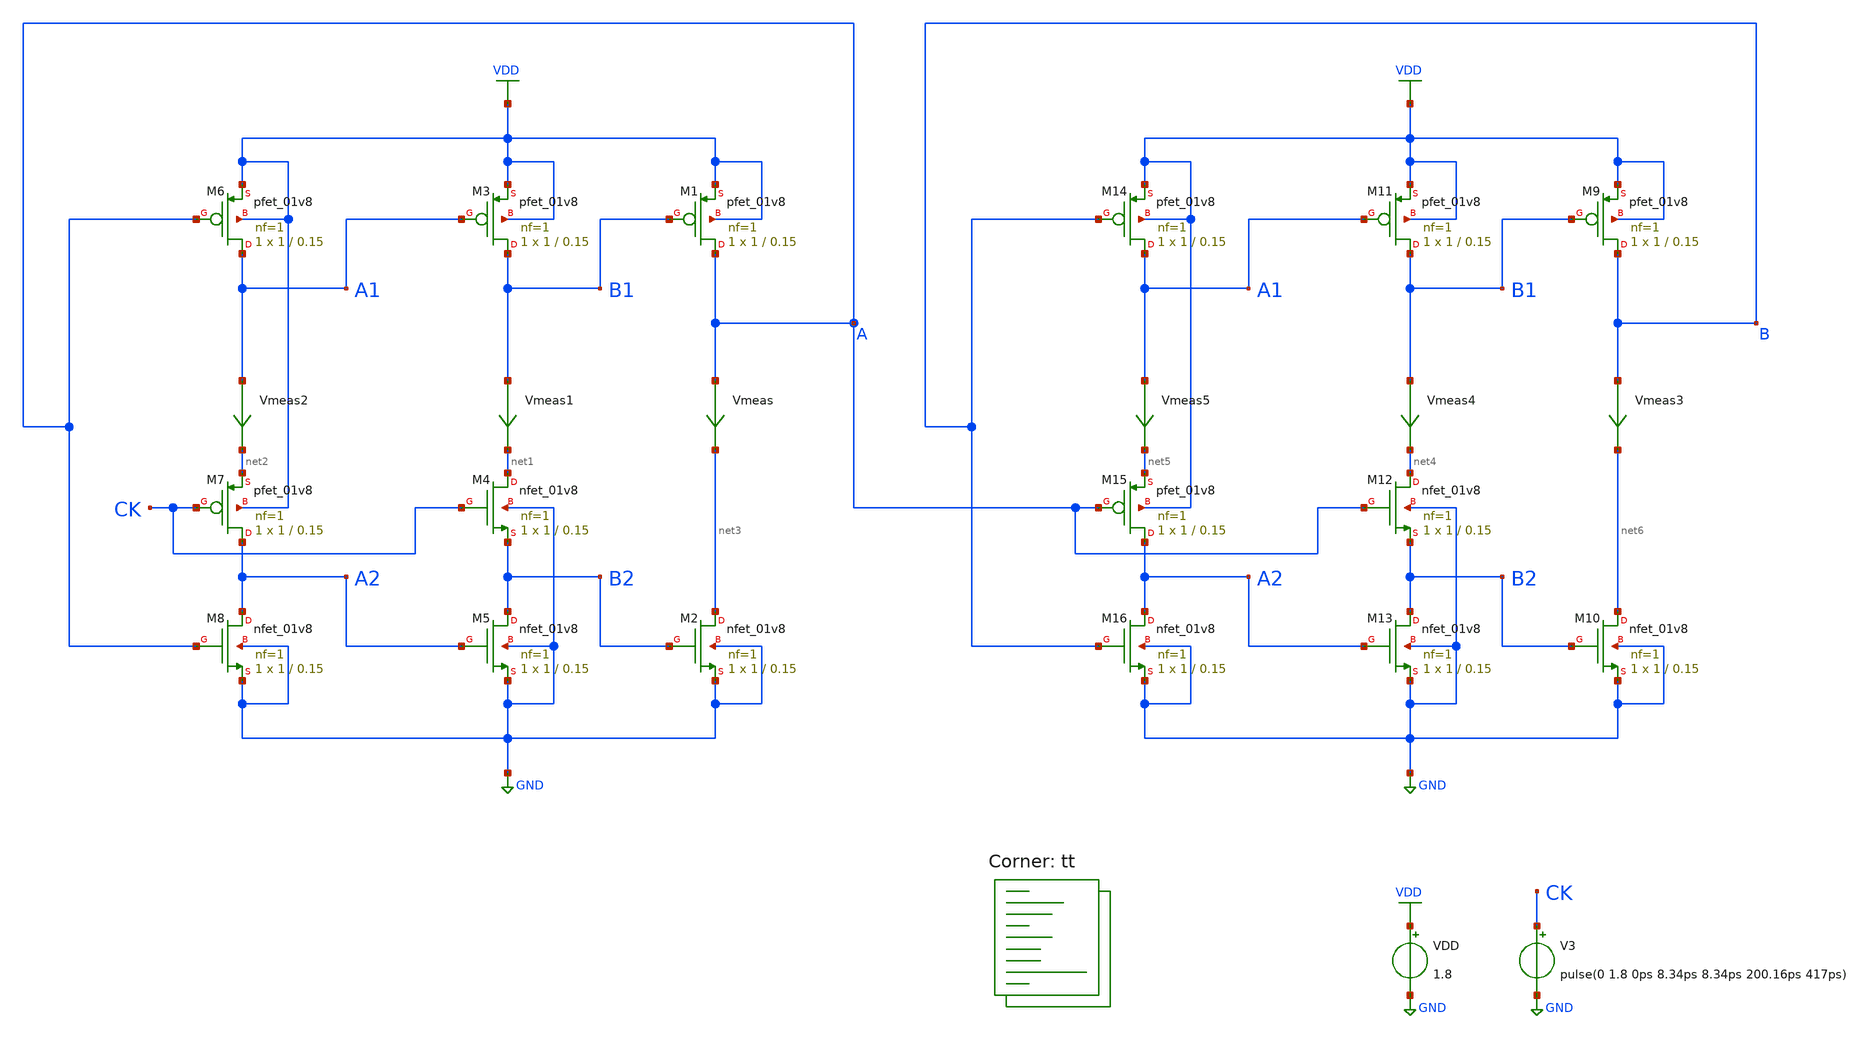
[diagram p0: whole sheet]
** sch_path: projects/pll/divider/xschem_ngspice/tb_TSPC_FF_split_path_2.sch
**.subckt tb_TSPC_FF_split_path_2
VDD VDD GND 1.8
V3 CK GND pulse(0 1.8 0ps 8.34ps 8.34ps 200.16ps 417ps)
XM1 A B1 VDD VDD sky130_fd_pr__pfet_01v8 L=0.15 W=1 nf=1 ad='int((nf+1)/2) * W/nf * 0.29' as='int((nf+2)/2) * W/nf * 0.29'
+ pd='2*int((nf+1)/2) * (W/nf + 0.29)' ps='2*int((nf+2)/2) * (W/nf + 0.29)' nrd='0.29 / W' nrs='0.29 / W'
+ sa=0 sb=0 sd=0 mult=1 m=1
XM4 net1 CK B2 GND sky130_fd_pr__nfet_01v8 L=0.15 W=1 nf=1 ad='int((nf+1)/2) * W/nf * 0.29' as='int((nf+2)/2) * W/nf * 0.29'
+ pd='2*int((nf+1)/2) * (W/nf + 0.29)' ps='2*int((nf+2)/2) * (W/nf + 0.29)' nrd='0.29 / W' nrs='0.29 / W'
+ sa=0 sb=0 sd=0 mult=1 m=1
Vmeas A net3 0
.save i(vmeas)
XM2 net3 B2 GND GND sky130_fd_pr__nfet_01v8 L=0.15 W=1 nf=1 ad='int((nf+1)/2) * W/nf * 0.29' as='int((nf+2)/2) * W/nf * 0.29'
+ pd='2*int((nf+1)/2) * (W/nf + 0.29)' ps='2*int((nf+2)/2) * (W/nf + 0.29)' nrd='0.29 / W' nrs='0.29 / W'
+ sa=0 sb=0 sd=0 mult=1 m=1
XM3 B1 A1 VDD VDD sky130_fd_pr__pfet_01v8 L=0.15 W=1 nf=1 ad='int((nf+1)/2) * W/nf * 0.29' as='int((nf+2)/2) * W/nf * 0.29'
+ pd='2*int((nf+1)/2) * (W/nf + 0.29)' ps='2*int((nf+2)/2) * (W/nf + 0.29)' nrd='0.29 / W' nrs='0.29 / W'
+ sa=0 sb=0 sd=0 mult=1 m=1
XM5 B2 A2 GND GND sky130_fd_pr__nfet_01v8 L=0.15 W=1 nf=1 ad='int((nf+1)/2) * W/nf * 0.29' as='int((nf+2)/2) * W/nf * 0.29'
+ pd='2*int((nf+1)/2) * (W/nf + 0.29)' ps='2*int((nf+2)/2) * (W/nf + 0.29)' nrd='0.29 / W' nrs='0.29 / W'
+ sa=0 sb=0 sd=0 mult=1 m=1
Vmeas1 B1 net1 0
.save i(vmeas1)
XM6 A1 A VDD VDD sky130_fd_pr__pfet_01v8 L=0.15 W=1 nf=1 ad='int((nf+1)/2) * W/nf * 0.29' as='int((nf+2)/2) * W/nf * 0.29'
+ pd='2*int((nf+1)/2) * (W/nf + 0.29)' ps='2*int((nf+2)/2) * (W/nf + 0.29)' nrd='0.29 / W' nrs='0.29 / W'
+ sa=0 sb=0 sd=0 mult=1 m=1
XM8 A2 A GND GND sky130_fd_pr__nfet_01v8 L=0.15 W=1 nf=1 ad='int((nf+1)/2) * W/nf * 0.29' as='int((nf+2)/2) * W/nf * 0.29'
+ pd='2*int((nf+1)/2) * (W/nf + 0.29)' ps='2*int((nf+2)/2) * (W/nf + 0.29)' nrd='0.29 / W' nrs='0.29 / W'
+ sa=0 sb=0 sd=0 mult=1 m=1
Vmeas2 A1 net2 0
.save i(vmeas2)
XM7 A2 CK net2 VDD sky130_fd_pr__pfet_01v8 L=0.15 W=1 nf=1 ad='int((nf+1)/2) * W/nf * 0.29' as='int((nf+2)/2) * W/nf * 0.29'
+ pd='2*int((nf+1)/2) * (W/nf + 0.29)' ps='2*int((nf+2)/2) * (W/nf + 0.29)' nrd='0.29 / W' nrs='0.29 / W'
+ sa=0 sb=0 sd=0 mult=1 m=1
XM9 B B1 VDD VDD sky130_fd_pr__pfet_01v8 L=0.15 W=1 nf=1 ad='int((nf+1)/2) * W/nf * 0.29' as='int((nf+2)/2) * W/nf * 0.29'
+ pd='2*int((nf+1)/2) * (W/nf + 0.29)' ps='2*int((nf+2)/2) * (W/nf + 0.29)' nrd='0.29 / W' nrs='0.29 / W'
+ sa=0 sb=0 sd=0 mult=1 m=1
XM12 net4 A B2 GND sky130_fd_pr__nfet_01v8 L=0.15 W=1 nf=1 ad='int((nf+1)/2) * W/nf * 0.29' as='int((nf+2)/2) * W/nf * 0.29'
+ pd='2*int((nf+1)/2) * (W/nf + 0.29)' ps='2*int((nf+2)/2) * (W/nf + 0.29)' nrd='0.29 / W' nrs='0.29 / W'
+ sa=0 sb=0 sd=0 mult=1 m=1
Vmeas3 B net6 0
.save i(vmeas3)
XM10 net6 B2 GND GND sky130_fd_pr__nfet_01v8 L=0.15 W=1 nf=1 ad='int((nf+1)/2) * W/nf * 0.29' as='int((nf+2)/2) * W/nf * 0.29'
+ pd='2*int((nf+1)/2) * (W/nf + 0.29)' ps='2*int((nf+2)/2) * (W/nf + 0.29)' nrd='0.29 / W' nrs='0.29 / W'
+ sa=0 sb=0 sd=0 mult=1 m=1
XM11 B1 A1 VDD VDD sky130_fd_pr__pfet_01v8 L=0.15 W=1 nf=1 ad='int((nf+1)/2) * W/nf * 0.29' as='int((nf+2)/2) * W/nf * 0.29'
+ pd='2*int((nf+1)/2) * (W/nf + 0.29)' ps='2*int((nf+2)/2) * (W/nf + 0.29)' nrd='0.29 / W' nrs='0.29 / W'
+ sa=0 sb=0 sd=0 mult=1 m=1
XM13 B2 A2 GND GND sky130_fd_pr__nfet_01v8 L=0.15 W=1 nf=1 ad='int((nf+1)/2) * W/nf * 0.29' as='int((nf+2)/2) * W/nf * 0.29'
+ pd='2*int((nf+1)/2) * (W/nf + 0.29)' ps='2*int((nf+2)/2) * (W/nf + 0.29)' nrd='0.29 / W' nrs='0.29 / W'
+ sa=0 sb=0 sd=0 mult=1 m=1
Vmeas4 B1 net4 0
.save i(vmeas4)
XM14 A1 B VDD VDD sky130_fd_pr__pfet_01v8 L=0.15 W=1 nf=1 ad='int((nf+1)/2) * W/nf * 0.29' as='int((nf+2)/2) * W/nf * 0.29'
+ pd='2*int((nf+1)/2) * (W/nf + 0.29)' ps='2*int((nf+2)/2) * (W/nf + 0.29)' nrd='0.29 / W' nrs='0.29 / W'
+ sa=0 sb=0 sd=0 mult=1 m=1
XM16 A2 B GND GND sky130_fd_pr__nfet_01v8 L=0.15 W=1 nf=1 ad='int((nf+1)/2) * W/nf * 0.29' as='int((nf+2)/2) * W/nf * 0.29'
+ pd='2*int((nf+1)/2) * (W/nf + 0.29)' ps='2*int((nf+2)/2) * (W/nf + 0.29)' nrd='0.29 / W' nrs='0.29 / W'
+ sa=0 sb=0 sd=0 mult=1 m=1
Vmeas5 A1 net5 0
.save i(vmeas5)
XM15 A2 A net5 VDD sky130_fd_pr__pfet_01v8 L=0.15 W=1 nf=1 ad='int((nf+1)/2) * W/nf * 0.29' as='int((nf+2)/2) * W/nf * 0.29'
+ pd='2*int((nf+1)/2) * (W/nf + 0.29)' ps='2*int((nf+2)/2) * (W/nf + 0.29)' nrd='0.29 / W' nrs='0.29 / W'
+ sa=0 sb=0 sd=0 mult=1 m=1
**** begin user architecture code



.include /foss/pdks/sky130A/libs.ref/sky130_fd_sc_hd/spice/sky130_fd_sc_hd.spice

.option method=gear
.option wnflag=1
* .option savecurrents

.save @m.xm1.msky130_fd_pr__pfet_01v8[gm] @m.xm2.msky130_fd_pr__nfet_01v8[gm] @m.xm3.msky130_fd_pr__pfet_01v8[gm] @m.xm4.msky130_fd_pr__nfet_01v8[gm] @m.xm5.msky130_fd_pr__nfet_01v8[gm] @m.xm6.msky130_fd_pr__pfet_01v8[gm] @m.xm7.msky130_fd_pr__pfet_01v8[gm] @m.xm8.msky130_fd_pr__nfet_01v8[gm]
 @m.xm9.msky130_fd_pr__pfet_01v8[gm] @m.xm10.msky130_fd_pr__nfet_01v8[gm]
+ @m.xm11.msky130_fd_pr__pfet_01v8[gm] @m.xm12.msky130_fd_pr__nfet_01v8[gm] @m.xm13.msky130_fd_pr__nfet_01v8[gm]
+ @m.xm14.msky130_fd_pr__pfet_01v8[gm] @m.xm15.msky130_fd_pr__pfet_01v8[gm] @m.xm16.msky130_fd_pr__nfet_01v8[gm]
 @v.vmeas @v.vmeas1 @v.vmeas2 @v.vmeas3 @v.vmeas4 @v.vmeas5


.control

  * save v(a) v(b) v(a1) v(b1) v(a2) v(b2) v(a3) v(b3) v(a4) v(b4) v(ck)
  save all
  *tran 0.1n 1u
  tran 0.2p 5n
  remzerovec
  write tb_TSPC_FF_split_path_2.raw
  set appendwrite

.endc



.lib $::SKYWATER_MODELS/sky130.lib.spice tt
**** end user architecture code
**.ends
.GLOBAL GND
.GLOBAL VDD
.end
